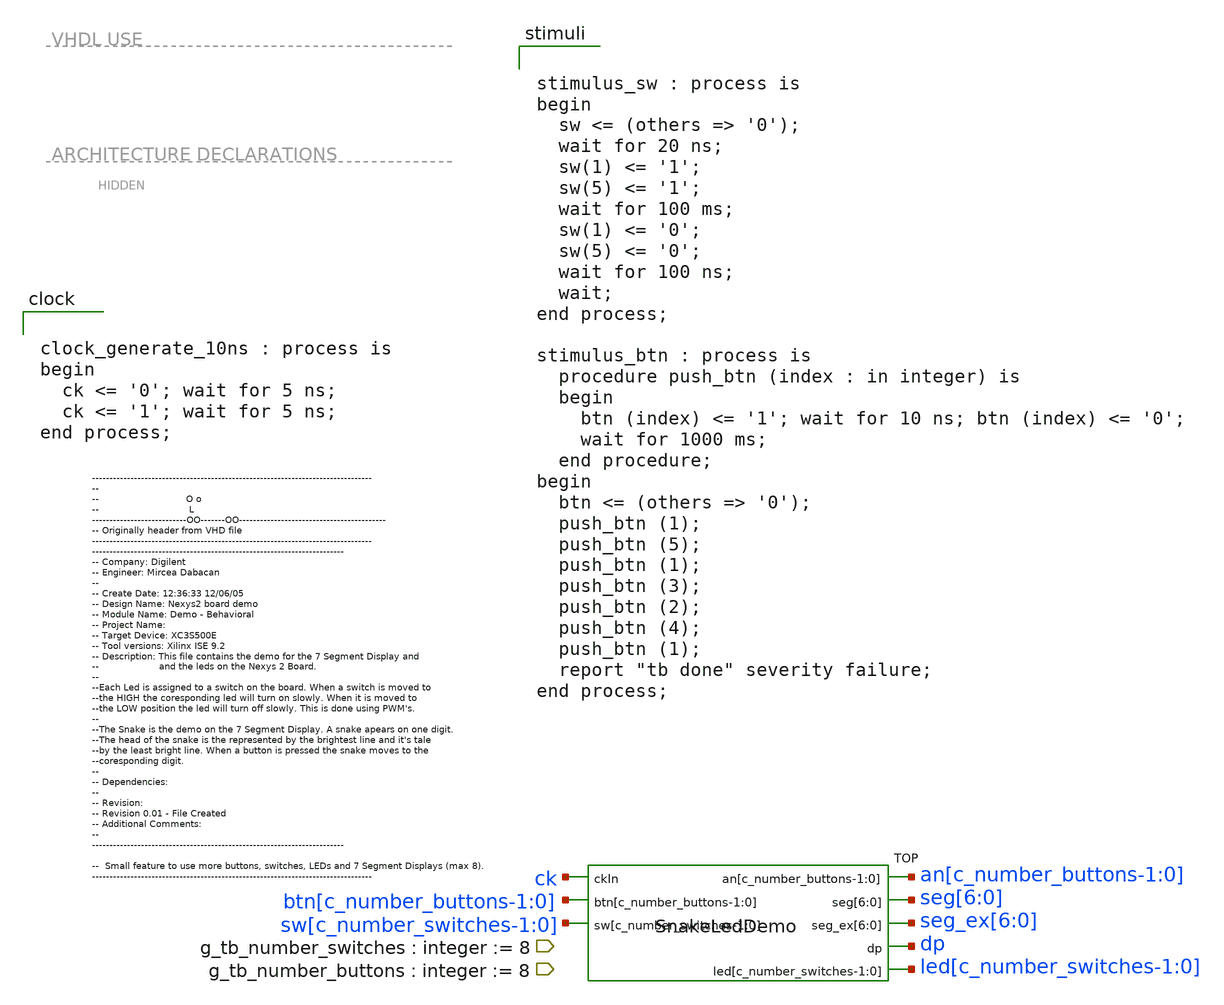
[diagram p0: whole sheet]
** sch_path: xschem/tb_SnakeLedDemo.sch
**.subckt tb_SnakeLedDemo
TOP an[c_number_buttons-1:0] ck seg[6] seg[5] seg[4] seg[3] seg[2] seg[1] seg[0]
+ btn[c_number_buttons-1:0] sw[c_number_switches-1:0] seg_ex[6] seg_ex[5] seg_ex[4] seg_ex[3] seg_ex[2] seg_ex[1] seg_ex[0] dp
+ led[c_number_switches-1:0] SnakeLedDemo
**** begin user architecture code


clock_generate_10ns : process is
begin
  ck <= '0'; wait for 5 ns;
  ck <= '1'; wait for 5 ns;
end process;




stimulus_sw : process is
begin
  sw <= (others => '0');
  wait for 20 ns;
  sw(1) <= '1';
  sw(5) <= '1';
  wait for 100 ms;
  sw(1) <= '0';
  sw(5) <= '0';
  wait for 100 ns;
  wait;
end process;

stimulus_btn : process is
  procedure push_btn (index : in integer) is
  begin
    btn (index) <= '1'; wait for 10 ns; btn (index) <= '0';
    wait for 1000 ms;
  end procedure;
begin
  btn <= (others => '0');
  push_btn (1);
  push_btn (5);
  push_btn (1);
  push_btn (3);
  push_btn (2);
  push_btn (4);
  push_btn (1);
  report "tb done" severity failure;
end process;


**** end user architecture code
**.ends

* expanding   symbol:  SnakeLedDemo.sym # of pins=8
** sym_path: xschem/SnakeLedDemo.sym
** sch_path: xschem/SnakeLedDemo.sch
.subckt SnakeLedDemo an[c_number_buttons-1:0] ckIn seg[6] seg[5] seg[4] seg[3] seg[2] seg[1] seg[0]
+ btn[c_number_buttons-1:0] sw[c_number_switches-1:0] seg_ex[6] seg_ex[5] seg_ex[4] seg_ex[3] seg_ex[2] seg_ex[1] seg_ex[0] dp
+ led[c_number_switches-1:0]
*.ipin ckIn
*.ipin sw[c_number_switches-1:0]
*.opin led[c_number_switches-1:0]
*.ipin btn[c_number_buttons-1:0]
*.opin an[c_number_buttons-1:0]
*.opin seg[6],seg[5],seg[4],seg[3],seg[2],seg[1],seg[0]
*.opin dp
*.opin seg_ex[6],seg_ex[5],seg_ex[4],seg_ex[3],seg_ex[2],seg_ex[1],seg_ex[0]
x1 cntDisp ck cntPwm[c_number_switches-1:0] ckFade cntDiv[c_ckSnake-1:0] ckSnake ClkDllDiv16
x2 cmpPwm sw[c_number_switches-1:0] ckFade ck Fadder
x3 cntPwm[c_number_switches-1:0] cmpPwm led[c_number_switches-1:0] PWM
x4 NextTarget ck ckSnake btn[c_number_buttons-1:0] NextTargetSet
x5 ck ckSnake Snake0 Target NextTarget Direction TargetSet
x6 Snake NextSnake ckSnake SnakeStateMachine
x7 ck btn[c_number_buttons-1:0] Direction NextTarget Target Snake NextSnake NextSnakeLogic
x8 cntDisp Snake0 Target an[c_number_buttons-1:0] anodeCtrl
x9 seg_ex[6] seg_ex[5] seg_ex[4] seg_ex[3] seg_ex[2] seg_ex[1] seg_ex[0] seg[6] seg[5] seg[4] seg[3]
+ seg[2] seg[1] seg[0] dp cntDisp segPwm[6] segPwm[5] segPwm[4] segPwm[3] segPwm[2] segPwm[1] segPwm[0]
+ Target Snake SegAssignment
**** begin user architecture code


segPwm(0) <= '0';
segPwm(1) <=
cntDiv(ckPwmRange) and
cntDiv(ckPwmRange+1);
segPwm(2) <=
cntDiv(ckPwmRange) ;
segPwm(3) <=
cntDiv(ckPwmRange) or
cntDiv(ckPwmRange+1);
segPwm(4) <=
cntDiv(ckPwmRange)
or cntDiv(ckPwmRange+1)
or cntDiv(ckPwmRange+2);
segPwm(5) <=
cntDiv(ckPwmRange) or
cntDiv(ckPwmRange+1) or
cntDiv(ckPwmRange+2) or
cntDiv(ckPwmRange+3);
segPwm(6) <=
cntDiv(ckPwmRange) or
cntDiv(ckPwmRange+1) or
cntDiv(ckPwmRange+2) or
cntDiv(ckPwmRange+3) or
cntDiv(ckPwmRange+4);


**** end user architecture code
**** begin user architecture code


IBUFG_ck : IBUFG port map (
  O => ck_ibufg,
  I => ckIn
);


**** end user architecture code
x11 ck ck_ibufg CLK_DLL
.ends


* expanding   symbol:  ClkDllDiv16.sym # of pins=6
** sym_path: xschem/ClkDllDiv16.sym
** sch_path: xschem/ClkDllDiv16.sch
.subckt ClkDllDiv16 cntDisp ckIn cntPwm[c_number_switches-1:0] ckFade cntDiv[c_ckSnake-1:0] ckSnake
*.ipin ckIn
*.opin cntDisp
*.opin cntPwm[c_number_switches-1:0]
*.opin ckFade
*.opin ckSnake
*.opin cntDiv[c_ckSnake-1:0]
**** begin user architecture code

p_ckDivider : process (ckIn) is
begin
  if rising_edge (ckIn) then
    cntDiv_i <= cntDiv_i + '1';
  end if;
end process;
cntPwm <= cntDiv_i (7 + ckPwmRange downto ckPwmRange);
ckFade <= cntDiv_i (c_ckFade - 1);
ckSnake <= cntDiv_i (c_ckSnake - 1);
ckAnode_i <= cntDiv_i (c_ckAnode - 1);
cntDiv <= cntDiv_i; -- XXX for cntPwm in top


**** end user architecture code
**** begin user architecture code


p_ckAnode : process (ckAnode_i) is
begin
  if ckAnode_i'event and ckAnode_i = '1' then
    if (cntDisp_i = c_number_buttons - 1) then
      cntDisp_i <= 0;
    else
      cntDisp_i <= cntDisp_i + 1;
    end if;
  end if;
end process;
cntDisp <= cntDisp_i;


**** end user architecture code
.ends


* expanding   symbol:  Fadder.sym # of pins=4
** sym_path: xschem/Fadder.sym
** sch_path: xschem/Fadder.sch
.subckt Fadder cmpPwm sw[c_number_switches-1:0] ckFade ck
*.ipin ck
*.ipin ckFade
*.ipin sw[c_number_switches-1:0]
*.iopin cmpPwm
**** begin user architecture code


p_Fadder : process (ckFade) is
begin
  for i in 0 to c_number_switches - 1 loop -- for each LED
    if ckFade'event and ckFade='1' then
      if sw(i) = '1' and cmpPwm(i) /= 255 then
        -- coresponding switch ON, not yet full intensity
        cmpPwm(i) <= cmpPwm(i)+1; -- increasing intensity
      elsif sw(i) = '0' and  cmpPwm(i) /= 0 then
        -- coresponding switch OFF, not yet full dark
        cmpPwm(i) <= cmpPwm(i)-1; -- decreasing intensity
      end if;
    end if;
  end loop;
end process;


**** end user architecture code
.ends


* expanding   symbol:  PWM.sym # of pins=3
** sym_path: xschem/PWM.sym
** sch_path: xschem/PWM.sch
.subckt PWM cntPwm[c_number_switches-1:0] cmpPwm Led[c_number_switches-1:0]
*.ipin cntPwm[c_number_switches-1:0]
*.ipin cmpPwm
*.opin Led[c_number_switches-1:0]
**** begin user architecture code


p_PWM : process (cntPwm, cmpPwm) is
begin
  for i in 0 to c_number_switches - 1 loop -- for each LED
    if conv_integer (cntPwm) < cmpPwm (i) then
      -- counter value less than reference
      Led(i) <= '1'; -- LED ON
    else
      -- counter value greater than reference
      Led(i) <= '0'; -- LED OFF
    end if;
  end loop;
end process;


**** end user architecture code
.ends


* expanding   symbol:  NextTargetSet.sym # of pins=4
** sym_path: xschem/NextTargetSet.sym
** sch_path: xschem/NextTargetSet.sch
.subckt NextTargetSet NextTarget ck ckSnake btn[c_number_buttons-1:0]
*.ipin ck
*.ipin ckSnake
*.ipin btn[c_number_buttons-1:0]
*.opin NextTarget
**** begin user architecture code


--in case a button is pressed sets the next target for the snake
p_NextTargetSet : process (ckSnake) is
begin
  if ckSnake'event and ckSnake='1' then
    for i in 0 to c_number_buttons - 1 loop
      if btn(i) = '1' then
        NextTarget <= i;
      end if;
    end loop;
  end if;
end process;


**** end user architecture code
.ends


* expanding   symbol:  TargetSet.sym # of pins=6
** sym_path: xschem/TargetSet.sym
** sch_path: xschem/TargetSet.sch
.subckt TargetSet ck ckSnake Snake Target NextTarget Direction
*.ipin Snake
*.opin Direction
*.ipin NextTarget
*.ipin ckSnake
*.ipin ck
*.iopin Target
**** begin user architecture code


p_TargetSet : process (ckSnake) is
begin
  if ckSnake'event and ckSnake='1' then
    if Snake(0) = (Target, 6) then -- already at target
      Target <= NextTarget;
      if NextTarget > Target then
        --sets the direction for the snake depending on
        --the position of the next target
        Direction <= left;
      elsif NextTarget < Target then
        Direction <= right;
      end if;
    end if;
  end if;
end process;


**** end user architecture code
.ends


* expanding   symbol:  SnakeStateMachine.sym # of pins=3
** sym_path: xschem/SnakeStateMachine.sym
** sch_path: xschem/SnakeStateMachine.sch
.subckt SnakeStateMachine Snake NextSnake ckSnake
*.opin Snake
*.ipin ckSnake
*.ipin NextSnake
**** begin user architecture code


p_SnakeStateMachine : process (ckSnake)
begin
	if ckSnake'event and ckSnake='1' then
		Snake <= NextSnake;
	end if;
end process;

**** end user architecture code
.ends


* expanding   symbol:  NextSnakeLogic.sym # of pins=7
** sym_path: xschem/NextSnakeLogic.sym
** sch_path: xschem/NextSnakeLogic.sch
.subckt NextSnakeLogic ck btn[c_number_buttons-1:0] Direction NextTarget Target Snake NextSnake
*.ipin ck
*.opin NextSnake
*.ipin Snake
*.ipin btn[c_number_buttons-1:0]
*.ipin Target
*.ipin Direction
*.ipin NextTarget
**** begin user architecture code


p_NextSnakeLogic : process (
  Target, nextTarget, Direction,
  Snake(0), Snake(1), Snake(2), Snake(3), Snake(4), Snake(5), Snake(6)
) is
begin
  if Snake(0) = (Target, 6) then -- already at target
    if    NextTarget > Target then
      NextSnake <= ((Target,6),(Target,1),(Target,0),(Target,5),(Target,4),(Target,3),(Target,2)); -- spinning to left
    elsif NextTarget < Target then
      NextSnake <= ((Target,6),(Target,5),(Target,0),(Target,1),(Target,2),(Target,3),(Target,4)); -- spinning to left
    else
      NextSnake <= Snake; -- resting
    end if;
  else -- snake moving
    NextSnake (1 to 6) <= Snake (0 to 5);
    if Direction = left then -- snake moving left
      if        Snake (0)  = (Target - 1    , 6)   then
            nextSnake (0) <= (Target        , 2);
      elsif     Snake (0)  = (Target        , 2)   then -- roling in target digit
            nextSnake (0) <= (Target        , 3);
      elsif     Snake (0)  = (Target        , 3)   then -- roling in target digit
            nextSnake (0) <= (Target        , 4);
      elsif     Snake (0)  = (Target        , 4)   then -- roling in target digit
            nextSnake (0) <= (Target        , 5);
      elsif     Snake (0)  = (Target        , 5)   then -- roling in target digit
            nextSnake (0) <= (Target        , 0);
      elsif     Snake (0)  = (Target        , 0)   then -- roling in target digit
            nextSnake (0) <= (Target        , 1);
      elsif     Snake (0)  = (Target        , 1)   then -- roling in target digit
            nextSnake (0) <= (Target        , 6);
      else
            nextsnake (0) <= Snake(0);
      end if;
      for i in c_number_buttons downto 2 loop
        if      Snake (0)  = (Target - i    , 6) then -- running to left
            NextSnake (0) <= (Target - i + 1, 6);
        end if;
      end loop;
    else -- snake moving right
      if        Snake (0)  = (Target + 1    , 6) then -- next right to target
            NextSnake (0) <= (Target        , 4);
      elsif     Snake (0)  = (Target        , 4) then -- roling in target digit
            NextSnake (0) <= (Target        , 3);
      elsif     Snake (0)  = (Target        , 3) then -- roling in target digit
            NextSnake (0) <= (Target        , 2);
      elsif     Snake (0)  = (Target        , 2) then -- roling in target digit
            NextSnake (0) <= (Target        , 1);
      elsif     Snake (0)  = (Target        , 1) then -- roling in target digit
            NextSnake (0) <= (Target        , 0);
      elsif     Snake (0)  = (Target        , 0) then -- roling in target digit
            NextSnake (0) <= (Target        , 5);
      elsif     Snake (0)  = (Target        , 5) then -- roling in target digit
            NextSnake (0) <= (Target        , 6);
      else
            NextSnake (0) <= Snake (6);
      end if;
      for i in c_number_buttons downto 2 loop
        if      Snake (0)  = (Target + i    , 6) then -- running to left
            NextSnake (0) <= (Target + i - 1, 6);
        end if;
      end loop;
    end if;
  end if;
end process;


**** end user architecture code
.ends


* expanding   symbol:  anodeCtrl.sym # of pins=4
** sym_path: xschem/anodeCtrl.sym
** sch_path: xschem/anodeCtrl.sch
.subckt anodeCtrl cntDisp Snake Target an[c_number_buttons-1:0]
*.ipin Target
*.ipin cntDisp
*.ipin Snake
*.opin an[c_number_buttons-1:0]
**** begin user architecture code


--Only one digit is active at a certain moment, this is done by activating one anodeat a time.
--The change of the active digits is done very fast and it makes you belive that all digits
--are lit at the same time
an <= an_i xor "00001111"; -- XXX for the maximator expander
p_anodeCtrl : process (cntDisp, Target, Snake(0))
	variable ones : std_logic_vector (c_number_buttons - 1 downto 0) := (others => '1');
begin
	an_i <= ones;
	for i in 0 to c_number_buttons - 1 loop
		if (Snake(0) = (Target, 6)) then
			an_i (Target) <= '0';
		elsif (cntDisp = i) then
			an_i (cntDisp) <= '0';
		end if;
	end loop;
end process;


**** end user architecture code
.ends


* expanding   symbol:  SegAssignment.sym # of pins=7
** sym_path: xschem/SegAssignment.sym
** sch_path: xschem/SegAssignment.sch
.subckt SegAssignment seg_ex[6] seg_ex[5] seg_ex[4] seg_ex[3] seg_ex[2] seg_ex[1] seg_ex[0] seg[6] seg[5] seg[4] seg[3] seg[2] seg[1] seg[0] dp cntDisp segPwm[6] segPwm[5] segPwm[4] segPwm[3] segPwm[2] segPwm[1] segPwm[0] Target Snake
*.ipin Snake
*.ipin cntDisp
*.opin seg[6],seg[5],seg[4],seg[3],seg[2],seg[1],seg[0]
*.ipin segPwm[6],segPwm[5],segPwm[4],segPwm[3],segPwm[2],segPwm[1],segPwm[0]
*.ipin Target
*.opin dp
*.opin seg_ex[6],seg_ex[5],seg_ex[4],seg_ex[3],seg_ex[2],seg_ex[1],seg_ex[0]
**** begin user architecture code


seg_ex <= seg_i xor "1111111"; -- XXX for the maximator expander
seg <= seg_i;
--The output segment vector is created here.
p_SegAssignment: process (
  cntDisp, segPwm, Target, Snake(0), Snake(1), Snake(2), Snake(3), Snake(4), Snake(5), Snake(6)
) is
begin
  seg_i <= "1111111";
  for k in 0 to 6 loop
    for i in 0 to 6 loop --loops all vertebras of the snake
      if Snake(i) = (cntDisp,k) then
        seg_i(k) <= segPwm(i);
      end if;
      if Target = cntDisp then -- current 7seg digit
        dp <= '0';  -- segment OFF
      else
        dp <= '1';	-- segment ON
      end if;
    end loop;
  end loop;
end process;


**** end user architecture code
.ends


* expanding   symbol:  CLK_DLL.sym # of pins=2
** sym_path: xschem/CLK_DLL.sym
** sch_path: xschem/CLK_DLL.sch
.subckt CLK_DLL ckOut ckIn
*.ipin ckIn
*.opin ckOut
**** begin user architecture code


CLK_DDL_BUFG_inst : BUFG port map (
  O => ckBuf2,
  I => ckBuf1
);

RST_SRL16_inst : SRL16
generic map (
  INIT => x"FFFF"
)
port map (
  D => '0',
  CLK => ckIn,
  A0 => '1',
  A1 => '1',
  A2 => '1',
  A3 => '1',
  Q => rst
);

CLK_DLL_inst : DCM port map (
  CLK0    => ckBuf1,
  CLKFB   => ckBuf2,
  CLKDV   => open,
  CLKIN   => ckIn,
  RST     => rst,
  CLK180  => open,
  CLK270  => open,
  CLK2X   => ckOut,
  CLK90   => open,
  LOCKED  => open
);


**** end user architecture code
.ends

.end
